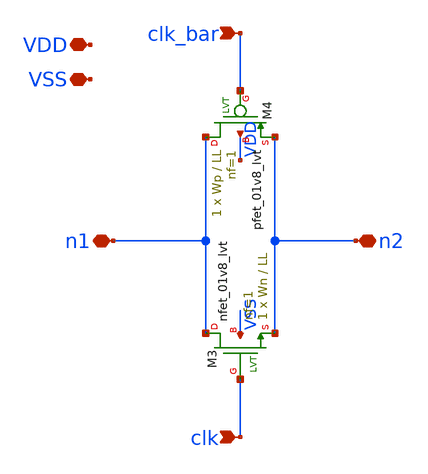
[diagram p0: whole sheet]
** sch_path: xschem/lib/Analog/TG_switch.sch
**.subckt TG_switch n2 n1 VDD VSS clk_bar clk
*.iopin n2
*.iopin n1
*.iopin VDD
*.iopin VSS
*.ipin clk_bar
*.ipin clk
XM3 n1 clk n2 VSS sky130_fd_pr__nfet_01v8_lvt L=LL W=Wn nf=1 ad='int((1 + 1)/2) * Wn / 1 * 0.29' as='int((1 + 2)/2) * Wn / 1 * 0.29'
+ pd='2*int((1 + 1)/2) * (Wn / 1 + 0.29)' ps='2*int((1 + 2)/2) * (Wn / 1 + 0.29)' nrd='0.29 / Wn ' nrs='0.29 / Wn '
+ sa=0 sb=0 sd=0 mult=1 m=1
XM4 n1 clk_bar n2 VDD sky130_fd_pr__pfet_01v8_lvt L=LL W=Wp nf=1 ad='int((1 + 1)/2) * Wp / 1 * 0.29'
+ as='int((1 + 2)/2) * Wp / 1 * 0.29' pd='2*int((1 + 1)/2) * (Wp / 1 + 0.29)' ps='2*int((1 + 2)/2) * (Wp / 1 + 0.29)'
+ nrd='0.29 / Wp ' nrs='0.29 / Wp ' sa=0 sb=0 sd=0 mult=1 m=1
**.ends
.end
